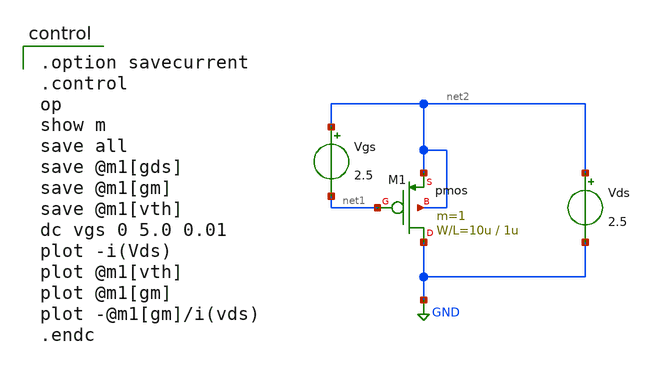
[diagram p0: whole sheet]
** sch_path: OR1/PTC06/opamp/pfet_idvgs.sch
**.subckt pfet_idvgs
Vgs net2 net1 2.5
Vds net2 GND 2.5
M1 GND net1 net2 net2 pmos L=1u W=10u m=1
**** begin user architecture code

.option savecurrent
.control
op
show m
save all
save @m1[gds]
save @m1[gm]
save @m1[vth]
dc vgs 0 5.0 0.01
plot -i(Vds)
plot @m1[vth]
plot @m1[gm]
plot -@m1[gm]/i(vds)
.endc

 .include $::LIB/mos.lib
.include $::LIB/passive.lib
.include $::LIB/diode.lib
**** end user architecture code
**.ends
.GLOBAL GND
.end
